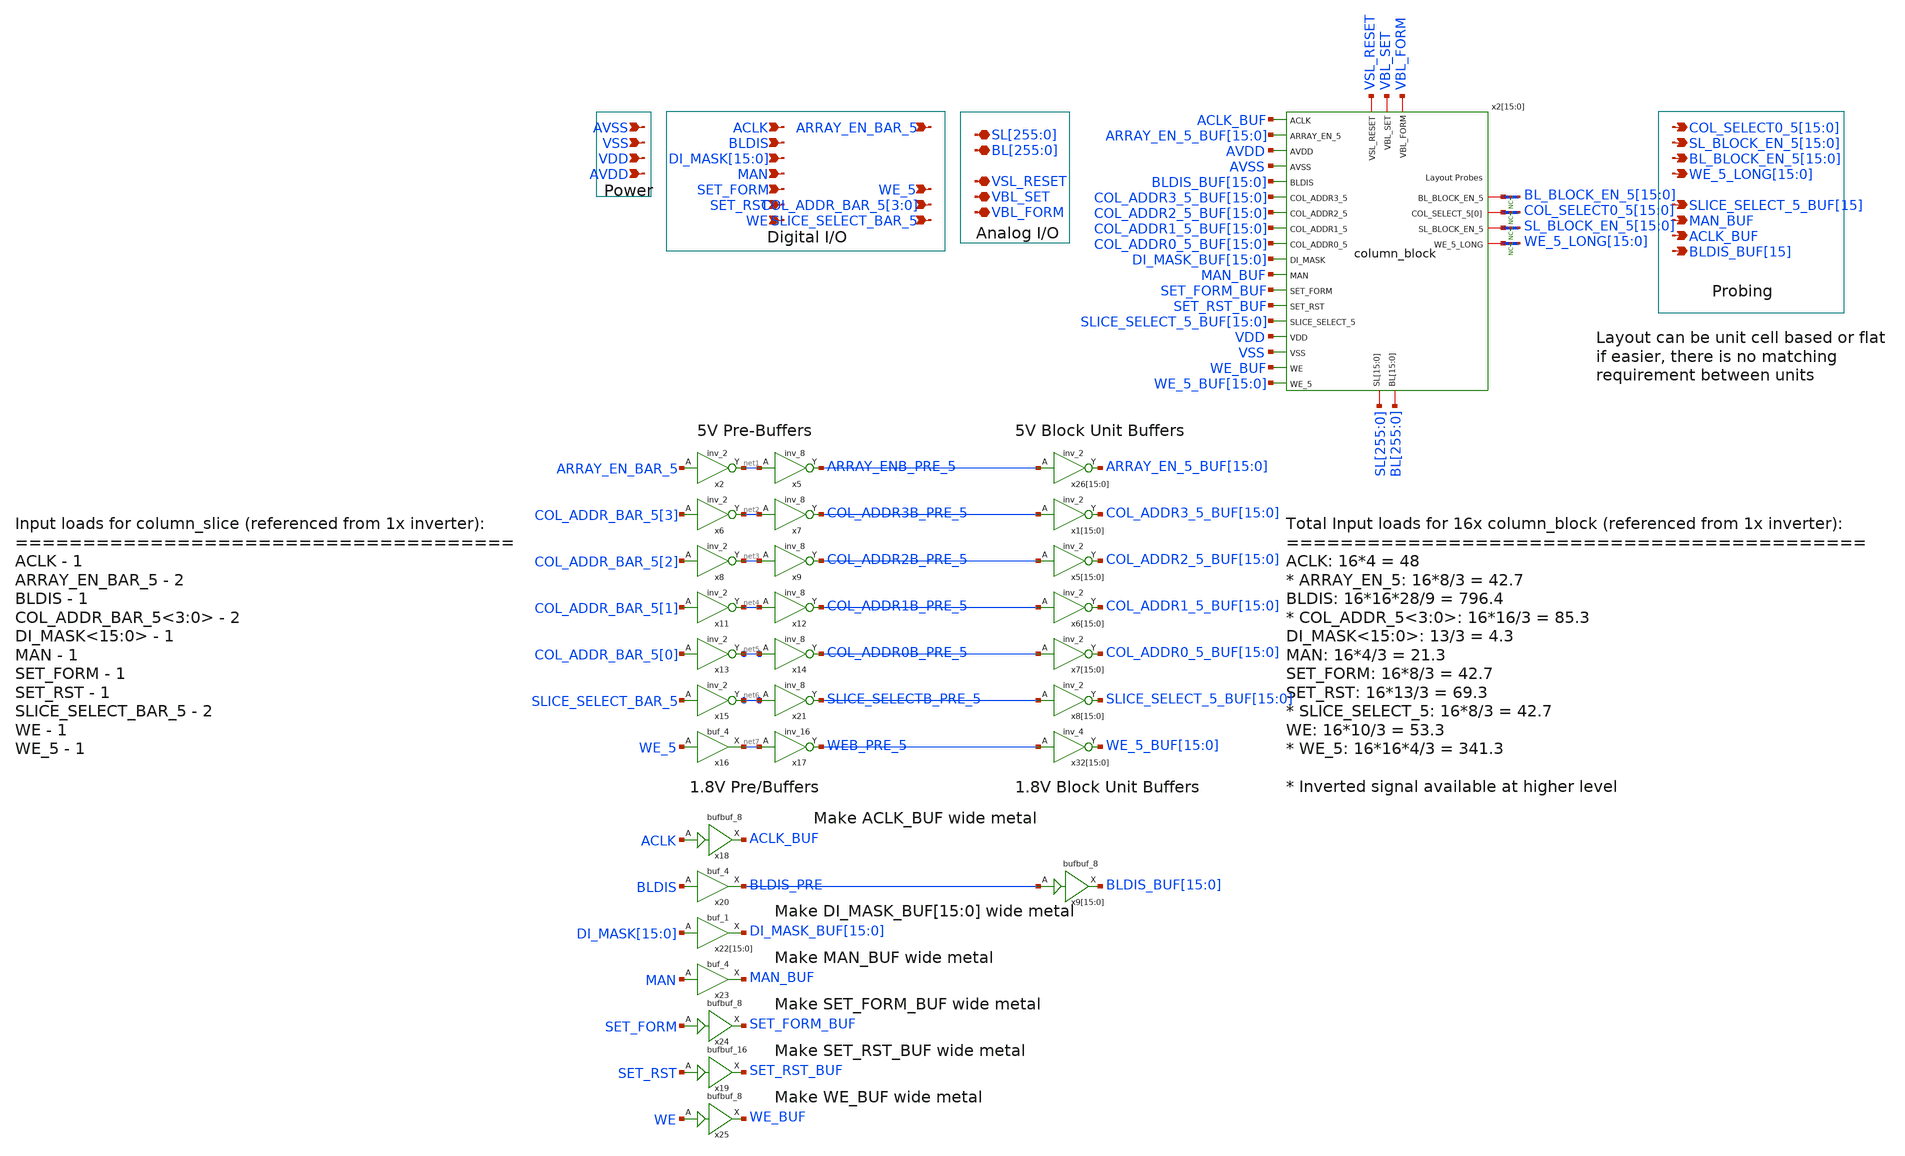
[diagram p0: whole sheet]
** sch_path: BL_SL_Writing_Interface/column_slice.sch
**.subckt column_slice
*+ COL_SELECT0_5[15],COL_SELECT0_5[14],COL_SELECT0_5[13],COL_SELECT0_5[12],COL_SELECT0_5[11],COL_SELECT0_5[10],COL_SELECT0_5[9],COL_SELECT0_5[8],COL_SELECT0_5[7],COL_SELECT0_5[6],COL_SELECT0_5[5],COL_SELECT0_5[4],COL_SELECT0_5[3],COL_SELECT0_5[2],COL_SELECT0_5[1],COL_SELECT0_5[0]
*+ SL_BLOCK_EN_5[15],SL_BLOCK_EN_5[14],SL_BLOCK_EN_5[13],SL_BLOCK_EN_5[12],SL_BLOCK_EN_5[11],SL_BLOCK_EN_5[10],SL_BLOCK_EN_5[9],SL_BLOCK_EN_5[8],SL_BLOCK_EN_5[7],SL_BLOCK_EN_5[6],SL_BLOCK_EN_5[5],SL_BLOCK_EN_5[4],SL_BLOCK_EN_5[3],SL_BLOCK_EN_5[2],SL_BLOCK_EN_5[1],SL_BLOCK_EN_5[0]
*+ BL_BLOCK_EN_5[15],BL_BLOCK_EN_5[14],BL_BLOCK_EN_5[13],BL_BLOCK_EN_5[12],BL_BLOCK_EN_5[11],BL_BLOCK_EN_5[10],BL_BLOCK_EN_5[9],BL_BLOCK_EN_5[8],BL_BLOCK_EN_5[7],BL_BLOCK_EN_5[6],BL_BLOCK_EN_5[5],BL_BLOCK_EN_5[4],BL_BLOCK_EN_5[3],BL_BLOCK_EN_5[2],BL_BLOCK_EN_5[1],BL_BLOCK_EN_5[0]
*+ WE_5_LONG[15],WE_5_LONG[14],WE_5_LONG[13],WE_5_LONG[12],WE_5_LONG[11],WE_5_LONG[10],WE_5_LONG[9],WE_5_LONG[8],WE_5_LONG[7],WE_5_LONG[6],WE_5_LONG[5],WE_5_LONG[4],WE_5_LONG[3],WE_5_LONG[2],WE_5_LONG[1],WE_5_LONG[0] SLICE_SELECT_5_BUF[15] MAN_BUF ACLK_BUF BLDIS_BUF[15]
*+ SL[255],SL[254],SL[253],SL[252],SL[251],SL[250],SL[249],SL[248],SL[247],SL[246],SL[245],SL[244],SL[243],SL[242],SL[241],SL[240],SL[239],SL[238],SL[237],SL[236],SL[235],SL[234],SL[233],SL[232],SL[231],SL[230],SL[229],SL[228],SL[227],SL[226],SL[225],SL[224],SL[223],SL[222],SL[221],SL[220],SL[219],SL[218],SL[217],SL[216],SL[215],SL[214],SL[213],SL[212],SL[211],SL[210],SL[209],SL[208],SL[207],SL[206],SL[205],SL[204],SL[203],SL[202],SL[201],SL[200],SL[199],SL[198],SL[197],SL[196],SL[195],SL[194],SL[193],SL[192],SL[191],SL[190],SL[189],SL[188],SL[187],SL[186],SL[185],SL[184],SL[183],SL[182],SL[181],SL[180],SL[179],SL[178],SL[177],SL[176],SL[175],SL[174],SL[173],SL[172],SL[171],SL[170],SL[169],SL[168],SL[167],SL[166],SL[165],SL[164],SL[163],SL[162],SL[161],SL[160],SL[159],SL[158],SL[157],SL[156],SL[155],SL[154],SL[153],SL[152],SL[151],SL[150],SL[149],SL[148],SL[147],SL[146],SL[145],SL[144],SL[143],SL[142],SL[141],SL[140],SL[139],SL[138],SL[137],SL[136],SL[135],SL[134],SL[133],SL[132],SL[131],SL[130],SL[129],SL[128],SL[127],SL[126],SL[125],SL[124],SL[123],SL[122],SL[121],SL[120],SL[119],SL[118],SL[117],SL[116],SL[115],SL[114],SL[113],SL[112],SL[111],SL[110],SL[109],SL[108],SL[107],SL[106],SL[105],SL[104],SL[103],SL[102],SL[101],SL[100],SL[99],SL[98],SL[97],SL[96],SL[95],SL[94],SL[93],SL[92],SL[91],SL[90],SL[89],SL[88],SL[87],SL[86],SL[85],SL[84],SL[83],SL[82],SL[81],SL[80],SL[79],SL[78],SL[77],SL[76],SL[75],SL[74],SL[73],SL[72],SL[71],SL[70],SL[69],SL[68],SL[67],SL[66],SL[65],SL[64],SL[63],SL[62],SL[61],SL[60],SL[59],SL[58],SL[57],SL[56],SL[55],SL[54],SL[53],SL[52],SL[51],SL[50],SL[49],SL[48],SL[47],SL[46],SL[45],SL[44],SL[43],SL[42],SL[41],SL[40],SL[39],SL[38],SL[37],SL[36],SL[35],SL[34],SL[33],SL[32],SL[31],SL[30],SL[29],SL[28],SL[27],SL[26],SL[25],SL[24],SL[23],SL[22],SL[21],SL[20],SL[19],SL[18],SL[17],SL[16],SL[15],SL[14],SL[13],SL[12],SL[11],SL[10],SL[9],SL[8],SL[7],SL[6],SL[5],SL[4],SL[3],SL[2],SL[1],SL[0]
*+ BL[255],BL[254],BL[253],BL[252],BL[251],BL[250],BL[249],BL[248],BL[247],BL[246],BL[245],BL[244],BL[243],BL[242],BL[241],BL[240],BL[239],BL[238],BL[237],BL[236],BL[235],BL[234],BL[233],BL[232],BL[231],BL[230],BL[229],BL[228],BL[227],BL[226],BL[225],BL[224],BL[223],BL[222],BL[221],BL[220],BL[219],BL[218],BL[217],BL[216],BL[215],BL[214],BL[213],BL[212],BL[211],BL[210],BL[209],BL[208],BL[207],BL[206],BL[205],BL[204],BL[203],BL[202],BL[201],BL[200],BL[199],BL[198],BL[197],BL[196],BL[195],BL[194],BL[193],BL[192],BL[191],BL[190],BL[189],BL[188],BL[187],BL[186],BL[185],BL[184],BL[183],BL[182],BL[181],BL[180],BL[179],BL[178],BL[177],BL[176],BL[175],BL[174],BL[173],BL[172],BL[171],BL[170],BL[169],BL[168],BL[167],BL[166],BL[165],BL[164],BL[163],BL[162],BL[161],BL[160],BL[159],BL[158],BL[157],BL[156],BL[155],BL[154],BL[153],BL[152],BL[151],BL[150],BL[149],BL[148],BL[147],BL[146],BL[145],BL[144],BL[143],BL[142],BL[141],BL[140],BL[139],BL[138],BL[137],BL[136],BL[135],BL[134],BL[133],BL[132],BL[131],BL[130],BL[129],BL[128],BL[127],BL[126],BL[125],BL[124],BL[123],BL[122],BL[121],BL[120],BL[119],BL[118],BL[117],BL[116],BL[115],BL[114],BL[113],BL[112],BL[111],BL[110],BL[109],BL[108],BL[107],BL[106],BL[105],BL[104],BL[103],BL[102],BL[101],BL[100],BL[99],BL[98],BL[97],BL[96],BL[95],BL[94],BL[93],BL[92],BL[91],BL[90],BL[89],BL[88],BL[87],BL[86],BL[85],BL[84],BL[83],BL[82],BL[81],BL[80],BL[79],BL[78],BL[77],BL[76],BL[75],BL[74],BL[73],BL[72],BL[71],BL[70],BL[69],BL[68],BL[67],BL[66],BL[65],BL[64],BL[63],BL[62],BL[61],BL[60],BL[59],BL[58],BL[57],BL[56],BL[55],BL[54],BL[53],BL[52],BL[51],BL[50],BL[49],BL[48],BL[47],BL[46],BL[45],BL[44],BL[43],BL[42],BL[41],BL[40],BL[39],BL[38],BL[37],BL[36],BL[35],BL[34],BL[33],BL[32],BL[31],BL[30],BL[29],BL[28],BL[27],BL[26],BL[25],BL[24],BL[23],BL[22],BL[21],BL[20],BL[19],BL[18],BL[17],BL[16],BL[15],BL[14],BL[13],BL[12],BL[11],BL[10],BL[9],BL[8],BL[7],BL[6],BL[5],BL[4],BL[3],BL[2],BL[1],BL[0] VSL_RESET VBL_SET VBL_FORM AVSS VSS VDD AVDD ACLK ARRAY_EN_BAR_5 BLDIS
*+ COL_ADDR_BAR_5[3],COL_ADDR_BAR_5[2],COL_ADDR_BAR_5[1],COL_ADDR_BAR_5[0]
*+ DI_MASK[15],DI_MASK[14],DI_MASK[13],DI_MASK[12],DI_MASK[11],DI_MASK[10],DI_MASK[9],DI_MASK[8],DI_MASK[7],DI_MASK[6],DI_MASK[5],DI_MASK[4],DI_MASK[3],DI_MASK[2],DI_MASK[1],DI_MASK[0] MAN WE SET_FORM SET_RST WE_5 SLICE_SELECT_BAR_5
*.opin
*+ COL_SELECT0_5[15],COL_SELECT0_5[14],COL_SELECT0_5[13],COL_SELECT0_5[12],COL_SELECT0_5[11],COL_SELECT0_5[10],COL_SELECT0_5[9],COL_SELECT0_5[8],COL_SELECT0_5[7],COL_SELECT0_5[6],COL_SELECT0_5[5],COL_SELECT0_5[4],COL_SELECT0_5[3],COL_SELECT0_5[2],COL_SELECT0_5[1],COL_SELECT0_5[0]
*.opin
*+ SL_BLOCK_EN_5[15],SL_BLOCK_EN_5[14],SL_BLOCK_EN_5[13],SL_BLOCK_EN_5[12],SL_BLOCK_EN_5[11],SL_BLOCK_EN_5[10],SL_BLOCK_EN_5[9],SL_BLOCK_EN_5[8],SL_BLOCK_EN_5[7],SL_BLOCK_EN_5[6],SL_BLOCK_EN_5[5],SL_BLOCK_EN_5[4],SL_BLOCK_EN_5[3],SL_BLOCK_EN_5[2],SL_BLOCK_EN_5[1],SL_BLOCK_EN_5[0]
*.opin
*+ BL_BLOCK_EN_5[15],BL_BLOCK_EN_5[14],BL_BLOCK_EN_5[13],BL_BLOCK_EN_5[12],BL_BLOCK_EN_5[11],BL_BLOCK_EN_5[10],BL_BLOCK_EN_5[9],BL_BLOCK_EN_5[8],BL_BLOCK_EN_5[7],BL_BLOCK_EN_5[6],BL_BLOCK_EN_5[5],BL_BLOCK_EN_5[4],BL_BLOCK_EN_5[3],BL_BLOCK_EN_5[2],BL_BLOCK_EN_5[1],BL_BLOCK_EN_5[0]
*.opin
*+ WE_5_LONG[15],WE_5_LONG[14],WE_5_LONG[13],WE_5_LONG[12],WE_5_LONG[11],WE_5_LONG[10],WE_5_LONG[9],WE_5_LONG[8],WE_5_LONG[7],WE_5_LONG[6],WE_5_LONG[5],WE_5_LONG[4],WE_5_LONG[3],WE_5_LONG[2],WE_5_LONG[1],WE_5_LONG[0]
*.opin SLICE_SELECT_5_BUF[15]
*.opin MAN_BUF
*.opin ACLK_BUF
*.opin BLDIS_BUF[15]
*.iopin
*+ SL[255],SL[254],SL[253],SL[252],SL[251],SL[250],SL[249],SL[248],SL[247],SL[246],SL[245],SL[244],SL[243],SL[242],SL[241],SL[240],SL[239],SL[238],SL[237],SL[236],SL[235],SL[234],SL[233],SL[232],SL[231],SL[230],SL[229],SL[228],SL[227],SL[226],SL[225],SL[224],SL[223],SL[222],SL[221],SL[220],SL[219],SL[218],SL[217],SL[216],SL[215],SL[214],SL[213],SL[212],SL[211],SL[210],SL[209],SL[208],SL[207],SL[206],SL[205],SL[204],SL[203],SL[202],SL[201],SL[200],SL[199],SL[198],SL[197],SL[196],SL[195],SL[194],SL[193],SL[192],SL[191],SL[190],SL[189],SL[188],SL[187],SL[186],SL[185],SL[184],SL[183],SL[182],SL[181],SL[180],SL[179],SL[178],SL[177],SL[176],SL[175],SL[174],SL[173],SL[172],SL[171],SL[170],SL[169],SL[168],SL[167],SL[166],SL[165],SL[164],SL[163],SL[162],SL[161],SL[160],SL[159],SL[158],SL[157],SL[156],SL[155],SL[154],SL[153],SL[152],SL[151],SL[150],SL[149],SL[148],SL[147],SL[146],SL[145],SL[144],SL[143],SL[142],SL[141],SL[140],SL[139],SL[138],SL[137],SL[136],SL[135],SL[134],SL[133],SL[132],SL[131],SL[130],SL[129],SL[128],SL[127],SL[126],SL[125],SL[124],SL[123],SL[122],SL[121],SL[120],SL[119],SL[118],SL[117],SL[116],SL[115],SL[114],SL[113],SL[112],SL[111],SL[110],SL[109],SL[108],SL[107],SL[106],SL[105],SL[104],SL[103],SL[102],SL[101],SL[100],SL[99],SL[98],SL[97],SL[96],SL[95],SL[94],SL[93],SL[92],SL[91],SL[90],SL[89],SL[88],SL[87],SL[86],SL[85],SL[84],SL[83],SL[82],SL[81],SL[80],SL[79],SL[78],SL[77],SL[76],SL[75],SL[74],SL[73],SL[72],SL[71],SL[70],SL[69],SL[68],SL[67],SL[66],SL[65],SL[64],SL[63],SL[62],SL[61],SL[60],SL[59],SL[58],SL[57],SL[56],SL[55],SL[54],SL[53],SL[52],SL[51],SL[50],SL[49],SL[48],SL[47],SL[46],SL[45],SL[44],SL[43],SL[42],SL[41],SL[40],SL[39],SL[38],SL[37],SL[36],SL[35],SL[34],SL[33],SL[32],SL[31],SL[30],SL[29],SL[28],SL[27],SL[26],SL[25],SL[24],SL[23],SL[22],SL[21],SL[20],SL[19],SL[18],SL[17],SL[16],SL[15],SL[14],SL[13],SL[12],SL[11],SL[10],SL[9],SL[8],SL[7],SL[6],SL[5],SL[4],SL[3],SL[2],SL[1],SL[0]
*.iopin
*+ BL[255],BL[254],BL[253],BL[252],BL[251],BL[250],BL[249],BL[248],BL[247],BL[246],BL[245],BL[244],BL[243],BL[242],BL[241],BL[240],BL[239],BL[238],BL[237],BL[236],BL[235],BL[234],BL[233],BL[232],BL[231],BL[230],BL[229],BL[228],BL[227],BL[226],BL[225],BL[224],BL[223],BL[222],BL[221],BL[220],BL[219],BL[218],BL[217],BL[216],BL[215],BL[214],BL[213],BL[212],BL[211],BL[210],BL[209],BL[208],BL[207],BL[206],BL[205],BL[204],BL[203],BL[202],BL[201],BL[200],BL[199],BL[198],BL[197],BL[196],BL[195],BL[194],BL[193],BL[192],BL[191],BL[190],BL[189],BL[188],BL[187],BL[186],BL[185],BL[184],BL[183],BL[182],BL[181],BL[180],BL[179],BL[178],BL[177],BL[176],BL[175],BL[174],BL[173],BL[172],BL[171],BL[170],BL[169],BL[168],BL[167],BL[166],BL[165],BL[164],BL[163],BL[162],BL[161],BL[160],BL[159],BL[158],BL[157],BL[156],BL[155],BL[154],BL[153],BL[152],BL[151],BL[150],BL[149],BL[148],BL[147],BL[146],BL[145],BL[144],BL[143],BL[142],BL[141],BL[140],BL[139],BL[138],BL[137],BL[136],BL[135],BL[134],BL[133],BL[132],BL[131],BL[130],BL[129],BL[128],BL[127],BL[126],BL[125],BL[124],BL[123],BL[122],BL[121],BL[120],BL[119],BL[118],BL[117],BL[116],BL[115],BL[114],BL[113],BL[112],BL[111],BL[110],BL[109],BL[108],BL[107],BL[106],BL[105],BL[104],BL[103],BL[102],BL[101],BL[100],BL[99],BL[98],BL[97],BL[96],BL[95],BL[94],BL[93],BL[92],BL[91],BL[90],BL[89],BL[88],BL[87],BL[86],BL[85],BL[84],BL[83],BL[82],BL[81],BL[80],BL[79],BL[78],BL[77],BL[76],BL[75],BL[74],BL[73],BL[72],BL[71],BL[70],BL[69],BL[68],BL[67],BL[66],BL[65],BL[64],BL[63],BL[62],BL[61],BL[60],BL[59],BL[58],BL[57],BL[56],BL[55],BL[54],BL[53],BL[52],BL[51],BL[50],BL[49],BL[48],BL[47],BL[46],BL[45],BL[44],BL[43],BL[42],BL[41],BL[40],BL[39],BL[38],BL[37],BL[36],BL[35],BL[34],BL[33],BL[32],BL[31],BL[30],BL[29],BL[28],BL[27],BL[26],BL[25],BL[24],BL[23],BL[22],BL[21],BL[20],BL[19],BL[18],BL[17],BL[16],BL[15],BL[14],BL[13],BL[12],BL[11],BL[10],BL[9],BL[8],BL[7],BL[6],BL[5],BL[4],BL[3],BL[2],BL[1],BL[0]
*.iopin VSL_RESET
*.iopin VBL_SET
*.iopin VBL_FORM
*.ipin AVSS
*.ipin VSS
*.ipin VDD
*.ipin AVDD
*.ipin ACLK
*.ipin ARRAY_EN_BAR_5
*.ipin BLDIS
*.ipin COL_ADDR_BAR_5[3],COL_ADDR_BAR_5[2],COL_ADDR_BAR_5[1],COL_ADDR_BAR_5[0]
*.ipin
*+ DI_MASK[15],DI_MASK[14],DI_MASK[13],DI_MASK[12],DI_MASK[11],DI_MASK[10],DI_MASK[9],DI_MASK[8],DI_MASK[7],DI_MASK[6],DI_MASK[5],DI_MASK[4],DI_MASK[3],DI_MASK[2],DI_MASK[1],DI_MASK[0]
*.ipin MAN
*.ipin WE
*.ipin SET_FORM
*.ipin SET_RST
*.ipin WE_5
*.ipin SLICE_SELECT_BAR_5
x2 ARRAY_EN_BAR_5 VSS VSS AVDD AVDD net1 sky130_fd_sc_hvl__inv_2
x5 net1 VSS VSS AVDD AVDD ARRAY_ENB_PRE_5 sky130_fd_sc_hvl__inv_8
x16 WE_5 VSS VSS AVDD AVDD net7 sky130_fd_sc_hvl__buf_4
x17 net7 VSS VSS AVDD AVDD WEB_PRE_5 sky130_fd_sc_hvl__inv_16
x18 ACLK VSS VSS VDD VDD ACLK_BUF sky130_fd_sc_hd__bufbuf_8
x19 SET_RST VSS VSS VDD VDD SET_RST_BUF sky130_fd_sc_hd__bufbuf_16
x6 COL_ADDR_BAR_5[3] VSS VSS AVDD AVDD net2 sky130_fd_sc_hvl__inv_2
x7 net2 VSS VSS AVDD AVDD COL_ADDR3B_PRE_5 sky130_fd_sc_hvl__inv_8
x8 COL_ADDR_BAR_5[2] VSS VSS AVDD AVDD net3 sky130_fd_sc_hvl__inv_2
x9 net3 VSS VSS AVDD AVDD COL_ADDR2B_PRE_5 sky130_fd_sc_hvl__inv_8
x11 COL_ADDR_BAR_5[1] VSS VSS AVDD AVDD net4 sky130_fd_sc_hvl__inv_2
x12 net4 VSS VSS AVDD AVDD COL_ADDR1B_PRE_5 sky130_fd_sc_hvl__inv_8
x13 COL_ADDR_BAR_5[0] VSS VSS AVDD AVDD net5 sky130_fd_sc_hvl__inv_2
x14 net5 VSS VSS AVDD AVDD COL_ADDR0B_PRE_5 sky130_fd_sc_hvl__inv_8
x15 SLICE_SELECT_BAR_5 VSS VSS AVDD AVDD net6 sky130_fd_sc_hvl__inv_2
x21 net6 VSS VSS AVDD AVDD SLICE_SELECTB_PRE_5 sky130_fd_sc_hvl__inv_8
x20 BLDIS VSS VSS VDD VDD BLDIS_PRE sky130_fd_sc_hd__buf_4
x22[15] DI_MASK[15] VSS VSS VDD VDD DI_MASK_BUF[15] sky130_fd_sc_hd__buf_1
x22[14] DI_MASK[14] VSS VSS VDD VDD DI_MASK_BUF[14] sky130_fd_sc_hd__buf_1
x22[13] DI_MASK[13] VSS VSS VDD VDD DI_MASK_BUF[13] sky130_fd_sc_hd__buf_1
x22[12] DI_MASK[12] VSS VSS VDD VDD DI_MASK_BUF[12] sky130_fd_sc_hd__buf_1
x22[11] DI_MASK[11] VSS VSS VDD VDD DI_MASK_BUF[11] sky130_fd_sc_hd__buf_1
x22[10] DI_MASK[10] VSS VSS VDD VDD DI_MASK_BUF[10] sky130_fd_sc_hd__buf_1
x22[9] DI_MASK[9] VSS VSS VDD VDD DI_MASK_BUF[9] sky130_fd_sc_hd__buf_1
x22[8] DI_MASK[8] VSS VSS VDD VDD DI_MASK_BUF[8] sky130_fd_sc_hd__buf_1
x22[7] DI_MASK[7] VSS VSS VDD VDD DI_MASK_BUF[7] sky130_fd_sc_hd__buf_1
x22[6] DI_MASK[6] VSS VSS VDD VDD DI_MASK_BUF[6] sky130_fd_sc_hd__buf_1
x22[5] DI_MASK[5] VSS VSS VDD VDD DI_MASK_BUF[5] sky130_fd_sc_hd__buf_1
x22[4] DI_MASK[4] VSS VSS VDD VDD DI_MASK_BUF[4] sky130_fd_sc_hd__buf_1
x22[3] DI_MASK[3] VSS VSS VDD VDD DI_MASK_BUF[3] sky130_fd_sc_hd__buf_1
x22[2] DI_MASK[2] VSS VSS VDD VDD DI_MASK_BUF[2] sky130_fd_sc_hd__buf_1
x22[1] DI_MASK[1] VSS VSS VDD VDD DI_MASK_BUF[1] sky130_fd_sc_hd__buf_1
x22[0] DI_MASK[0] VSS VSS VDD VDD DI_MASK_BUF[0] sky130_fd_sc_hd__buf_1
x23 MAN VSS VSS VDD VDD MAN_BUF sky130_fd_sc_hd__buf_4
x24 SET_FORM VSS VSS VDD VDD SET_FORM_BUF sky130_fd_sc_hd__bufbuf_8
x25 WE VSS VSS VDD VDD WE_BUF sky130_fd_sc_hd__bufbuf_8
x26[15] ARRAY_ENB_PRE_5 VSS VSS AVDD AVDD ARRAY_EN_5_BUF[15] sky130_fd_sc_hvl__inv_2
x26[14] ARRAY_ENB_PRE_5 VSS VSS AVDD AVDD ARRAY_EN_5_BUF[14] sky130_fd_sc_hvl__inv_2
x26[13] ARRAY_ENB_PRE_5 VSS VSS AVDD AVDD ARRAY_EN_5_BUF[13] sky130_fd_sc_hvl__inv_2
x26[12] ARRAY_ENB_PRE_5 VSS VSS AVDD AVDD ARRAY_EN_5_BUF[12] sky130_fd_sc_hvl__inv_2
x26[11] ARRAY_ENB_PRE_5 VSS VSS AVDD AVDD ARRAY_EN_5_BUF[11] sky130_fd_sc_hvl__inv_2
x26[10] ARRAY_ENB_PRE_5 VSS VSS AVDD AVDD ARRAY_EN_5_BUF[10] sky130_fd_sc_hvl__inv_2
x26[9] ARRAY_ENB_PRE_5 VSS VSS AVDD AVDD ARRAY_EN_5_BUF[9] sky130_fd_sc_hvl__inv_2
x26[8] ARRAY_ENB_PRE_5 VSS VSS AVDD AVDD ARRAY_EN_5_BUF[8] sky130_fd_sc_hvl__inv_2
x26[7] ARRAY_ENB_PRE_5 VSS VSS AVDD AVDD ARRAY_EN_5_BUF[7] sky130_fd_sc_hvl__inv_2
x26[6] ARRAY_ENB_PRE_5 VSS VSS AVDD AVDD ARRAY_EN_5_BUF[6] sky130_fd_sc_hvl__inv_2
x26[5] ARRAY_ENB_PRE_5 VSS VSS AVDD AVDD ARRAY_EN_5_BUF[5] sky130_fd_sc_hvl__inv_2
x26[4] ARRAY_ENB_PRE_5 VSS VSS AVDD AVDD ARRAY_EN_5_BUF[4] sky130_fd_sc_hvl__inv_2
x26[3] ARRAY_ENB_PRE_5 VSS VSS AVDD AVDD ARRAY_EN_5_BUF[3] sky130_fd_sc_hvl__inv_2
x26[2] ARRAY_ENB_PRE_5 VSS VSS AVDD AVDD ARRAY_EN_5_BUF[2] sky130_fd_sc_hvl__inv_2
x26[1] ARRAY_ENB_PRE_5 VSS VSS AVDD AVDD ARRAY_EN_5_BUF[1] sky130_fd_sc_hvl__inv_2
x26[0] ARRAY_ENB_PRE_5 VSS VSS AVDD AVDD ARRAY_EN_5_BUF[0] sky130_fd_sc_hvl__inv_2
x32[15] WEB_PRE_5 VGND VNB VPB VPWR WE_5_BUF[15] sky130_fd_sc_hvl__inv_4
x32[14] WEB_PRE_5 VGND VNB VPB VPWR WE_5_BUF[14] sky130_fd_sc_hvl__inv_4
x32[13] WEB_PRE_5 VGND VNB VPB VPWR WE_5_BUF[13] sky130_fd_sc_hvl__inv_4
x32[12] WEB_PRE_5 VGND VNB VPB VPWR WE_5_BUF[12] sky130_fd_sc_hvl__inv_4
x32[11] WEB_PRE_5 VGND VNB VPB VPWR WE_5_BUF[11] sky130_fd_sc_hvl__inv_4
x32[10] WEB_PRE_5 VGND VNB VPB VPWR WE_5_BUF[10] sky130_fd_sc_hvl__inv_4
x32[9] WEB_PRE_5 VGND VNB VPB VPWR WE_5_BUF[9] sky130_fd_sc_hvl__inv_4
x32[8] WEB_PRE_5 VGND VNB VPB VPWR WE_5_BUF[8] sky130_fd_sc_hvl__inv_4
x32[7] WEB_PRE_5 VGND VNB VPB VPWR WE_5_BUF[7] sky130_fd_sc_hvl__inv_4
x32[6] WEB_PRE_5 VGND VNB VPB VPWR WE_5_BUF[6] sky130_fd_sc_hvl__inv_4
x32[5] WEB_PRE_5 VGND VNB VPB VPWR WE_5_BUF[5] sky130_fd_sc_hvl__inv_4
x32[4] WEB_PRE_5 VGND VNB VPB VPWR WE_5_BUF[4] sky130_fd_sc_hvl__inv_4
x32[3] WEB_PRE_5 VGND VNB VPB VPWR WE_5_BUF[3] sky130_fd_sc_hvl__inv_4
x32[2] WEB_PRE_5 VGND VNB VPB VPWR WE_5_BUF[2] sky130_fd_sc_hvl__inv_4
x32[1] WEB_PRE_5 VGND VNB VPB VPWR WE_5_BUF[1] sky130_fd_sc_hvl__inv_4
x32[0] WEB_PRE_5 VGND VNB VPB VPWR WE_5_BUF[0] sky130_fd_sc_hvl__inv_4
x1[15] COL_ADDR3B_PRE_5 VSS VSS AVDD AVDD COL_ADDR3_5_BUF[15] sky130_fd_sc_hvl__inv_2
x1[14] COL_ADDR3B_PRE_5 VSS VSS AVDD AVDD COL_ADDR3_5_BUF[14] sky130_fd_sc_hvl__inv_2
x1[13] COL_ADDR3B_PRE_5 VSS VSS AVDD AVDD COL_ADDR3_5_BUF[13] sky130_fd_sc_hvl__inv_2
x1[12] COL_ADDR3B_PRE_5 VSS VSS AVDD AVDD COL_ADDR3_5_BUF[12] sky130_fd_sc_hvl__inv_2
x1[11] COL_ADDR3B_PRE_5 VSS VSS AVDD AVDD COL_ADDR3_5_BUF[11] sky130_fd_sc_hvl__inv_2
x1[10] COL_ADDR3B_PRE_5 VSS VSS AVDD AVDD COL_ADDR3_5_BUF[10] sky130_fd_sc_hvl__inv_2
x1[9] COL_ADDR3B_PRE_5 VSS VSS AVDD AVDD COL_ADDR3_5_BUF[9] sky130_fd_sc_hvl__inv_2
x1[8] COL_ADDR3B_PRE_5 VSS VSS AVDD AVDD COL_ADDR3_5_BUF[8] sky130_fd_sc_hvl__inv_2
x1[7] COL_ADDR3B_PRE_5 VSS VSS AVDD AVDD COL_ADDR3_5_BUF[7] sky130_fd_sc_hvl__inv_2
x1[6] COL_ADDR3B_PRE_5 VSS VSS AVDD AVDD COL_ADDR3_5_BUF[6] sky130_fd_sc_hvl__inv_2
x1[5] COL_ADDR3B_PRE_5 VSS VSS AVDD AVDD COL_ADDR3_5_BUF[5] sky130_fd_sc_hvl__inv_2
x1[4] COL_ADDR3B_PRE_5 VSS VSS AVDD AVDD COL_ADDR3_5_BUF[4] sky130_fd_sc_hvl__inv_2
x1[3] COL_ADDR3B_PRE_5 VSS VSS AVDD AVDD COL_ADDR3_5_BUF[3] sky130_fd_sc_hvl__inv_2
x1[2] COL_ADDR3B_PRE_5 VSS VSS AVDD AVDD COL_ADDR3_5_BUF[2] sky130_fd_sc_hvl__inv_2
x1[1] COL_ADDR3B_PRE_5 VSS VSS AVDD AVDD COL_ADDR3_5_BUF[1] sky130_fd_sc_hvl__inv_2
x1[0] COL_ADDR3B_PRE_5 VSS VSS AVDD AVDD COL_ADDR3_5_BUF[0] sky130_fd_sc_hvl__inv_2
x5[15] COL_ADDR2B_PRE_5 VSS VSS AVDD AVDD COL_ADDR2_5_BUF[15] sky130_fd_sc_hvl__inv_2
x5[14] COL_ADDR2B_PRE_5 VSS VSS AVDD AVDD COL_ADDR2_5_BUF[14] sky130_fd_sc_hvl__inv_2
x5[13] COL_ADDR2B_PRE_5 VSS VSS AVDD AVDD COL_ADDR2_5_BUF[13] sky130_fd_sc_hvl__inv_2
x5[12] COL_ADDR2B_PRE_5 VSS VSS AVDD AVDD COL_ADDR2_5_BUF[12] sky130_fd_sc_hvl__inv_2
x5[11] COL_ADDR2B_PRE_5 VSS VSS AVDD AVDD COL_ADDR2_5_BUF[11] sky130_fd_sc_hvl__inv_2
x5[10] COL_ADDR2B_PRE_5 VSS VSS AVDD AVDD COL_ADDR2_5_BUF[10] sky130_fd_sc_hvl__inv_2
x5[9] COL_ADDR2B_PRE_5 VSS VSS AVDD AVDD COL_ADDR2_5_BUF[9] sky130_fd_sc_hvl__inv_2
x5[8] COL_ADDR2B_PRE_5 VSS VSS AVDD AVDD COL_ADDR2_5_BUF[8] sky130_fd_sc_hvl__inv_2
x5[7] COL_ADDR2B_PRE_5 VSS VSS AVDD AVDD COL_ADDR2_5_BUF[7] sky130_fd_sc_hvl__inv_2
x5[6] COL_ADDR2B_PRE_5 VSS VSS AVDD AVDD COL_ADDR2_5_BUF[6] sky130_fd_sc_hvl__inv_2
x5[5] COL_ADDR2B_PRE_5 VSS VSS AVDD AVDD COL_ADDR2_5_BUF[5] sky130_fd_sc_hvl__inv_2
x5[4] COL_ADDR2B_PRE_5 VSS VSS AVDD AVDD COL_ADDR2_5_BUF[4] sky130_fd_sc_hvl__inv_2
x5[3] COL_ADDR2B_PRE_5 VSS VSS AVDD AVDD COL_ADDR2_5_BUF[3] sky130_fd_sc_hvl__inv_2
x5[2] COL_ADDR2B_PRE_5 VSS VSS AVDD AVDD COL_ADDR2_5_BUF[2] sky130_fd_sc_hvl__inv_2
x5[1] COL_ADDR2B_PRE_5 VSS VSS AVDD AVDD COL_ADDR2_5_BUF[1] sky130_fd_sc_hvl__inv_2
x5[0] COL_ADDR2B_PRE_5 VSS VSS AVDD AVDD COL_ADDR2_5_BUF[0] sky130_fd_sc_hvl__inv_2
x6[15] COL_ADDR1B_PRE_5 VSS VSS AVDD AVDD COL_ADDR1_5_BUF[15] sky130_fd_sc_hvl__inv_2
x6[14] COL_ADDR1B_PRE_5 VSS VSS AVDD AVDD COL_ADDR1_5_BUF[14] sky130_fd_sc_hvl__inv_2
x6[13] COL_ADDR1B_PRE_5 VSS VSS AVDD AVDD COL_ADDR1_5_BUF[13] sky130_fd_sc_hvl__inv_2
x6[12] COL_ADDR1B_PRE_5 VSS VSS AVDD AVDD COL_ADDR1_5_BUF[12] sky130_fd_sc_hvl__inv_2
x6[11] COL_ADDR1B_PRE_5 VSS VSS AVDD AVDD COL_ADDR1_5_BUF[11] sky130_fd_sc_hvl__inv_2
x6[10] COL_ADDR1B_PRE_5 VSS VSS AVDD AVDD COL_ADDR1_5_BUF[10] sky130_fd_sc_hvl__inv_2
x6[9] COL_ADDR1B_PRE_5 VSS VSS AVDD AVDD COL_ADDR1_5_BUF[9] sky130_fd_sc_hvl__inv_2
x6[8] COL_ADDR1B_PRE_5 VSS VSS AVDD AVDD COL_ADDR1_5_BUF[8] sky130_fd_sc_hvl__inv_2
x6[7] COL_ADDR1B_PRE_5 VSS VSS AVDD AVDD COL_ADDR1_5_BUF[7] sky130_fd_sc_hvl__inv_2
x6[6] COL_ADDR1B_PRE_5 VSS VSS AVDD AVDD COL_ADDR1_5_BUF[6] sky130_fd_sc_hvl__inv_2
x6[5] COL_ADDR1B_PRE_5 VSS VSS AVDD AVDD COL_ADDR1_5_BUF[5] sky130_fd_sc_hvl__inv_2
x6[4] COL_ADDR1B_PRE_5 VSS VSS AVDD AVDD COL_ADDR1_5_BUF[4] sky130_fd_sc_hvl__inv_2
x6[3] COL_ADDR1B_PRE_5 VSS VSS AVDD AVDD COL_ADDR1_5_BUF[3] sky130_fd_sc_hvl__inv_2
x6[2] COL_ADDR1B_PRE_5 VSS VSS AVDD AVDD COL_ADDR1_5_BUF[2] sky130_fd_sc_hvl__inv_2
x6[1] COL_ADDR1B_PRE_5 VSS VSS AVDD AVDD COL_ADDR1_5_BUF[1] sky130_fd_sc_hvl__inv_2
x6[0] COL_ADDR1B_PRE_5 VSS VSS AVDD AVDD COL_ADDR1_5_BUF[0] sky130_fd_sc_hvl__inv_2
x7[15] COL_ADDR0B_PRE_5 VSS VSS AVDD AVDD COL_ADDR0_5_BUF[15] sky130_fd_sc_hvl__inv_2
x7[14] COL_ADDR0B_PRE_5 VSS VSS AVDD AVDD COL_ADDR0_5_BUF[14] sky130_fd_sc_hvl__inv_2
x7[13] COL_ADDR0B_PRE_5 VSS VSS AVDD AVDD COL_ADDR0_5_BUF[13] sky130_fd_sc_hvl__inv_2
x7[12] COL_ADDR0B_PRE_5 VSS VSS AVDD AVDD COL_ADDR0_5_BUF[12] sky130_fd_sc_hvl__inv_2
x7[11] COL_ADDR0B_PRE_5 VSS VSS AVDD AVDD COL_ADDR0_5_BUF[11] sky130_fd_sc_hvl__inv_2
x7[10] COL_ADDR0B_PRE_5 VSS VSS AVDD AVDD COL_ADDR0_5_BUF[10] sky130_fd_sc_hvl__inv_2
x7[9] COL_ADDR0B_PRE_5 VSS VSS AVDD AVDD COL_ADDR0_5_BUF[9] sky130_fd_sc_hvl__inv_2
x7[8] COL_ADDR0B_PRE_5 VSS VSS AVDD AVDD COL_ADDR0_5_BUF[8] sky130_fd_sc_hvl__inv_2
x7[7] COL_ADDR0B_PRE_5 VSS VSS AVDD AVDD COL_ADDR0_5_BUF[7] sky130_fd_sc_hvl__inv_2
x7[6] COL_ADDR0B_PRE_5 VSS VSS AVDD AVDD COL_ADDR0_5_BUF[6] sky130_fd_sc_hvl__inv_2
x7[5] COL_ADDR0B_PRE_5 VSS VSS AVDD AVDD COL_ADDR0_5_BUF[5] sky130_fd_sc_hvl__inv_2
x7[4] COL_ADDR0B_PRE_5 VSS VSS AVDD AVDD COL_ADDR0_5_BUF[4] sky130_fd_sc_hvl__inv_2
x7[3] COL_ADDR0B_PRE_5 VSS VSS AVDD AVDD COL_ADDR0_5_BUF[3] sky130_fd_sc_hvl__inv_2
x7[2] COL_ADDR0B_PRE_5 VSS VSS AVDD AVDD COL_ADDR0_5_BUF[2] sky130_fd_sc_hvl__inv_2
x7[1] COL_ADDR0B_PRE_5 VSS VSS AVDD AVDD COL_ADDR0_5_BUF[1] sky130_fd_sc_hvl__inv_2
x7[0] COL_ADDR0B_PRE_5 VSS VSS AVDD AVDD COL_ADDR0_5_BUF[0] sky130_fd_sc_hvl__inv_2
x8[15] SLICE_SELECTB_PRE_5 VSS VSS AVDD AVDD SLICE_SELECT_5_BUF[15] sky130_fd_sc_hvl__inv_2
x8[14] SLICE_SELECTB_PRE_5 VSS VSS AVDD AVDD SLICE_SELECT_5_BUF[14] sky130_fd_sc_hvl__inv_2
x8[13] SLICE_SELECTB_PRE_5 VSS VSS AVDD AVDD SLICE_SELECT_5_BUF[13] sky130_fd_sc_hvl__inv_2
x8[12] SLICE_SELECTB_PRE_5 VSS VSS AVDD AVDD SLICE_SELECT_5_BUF[12] sky130_fd_sc_hvl__inv_2
x8[11] SLICE_SELECTB_PRE_5 VSS VSS AVDD AVDD SLICE_SELECT_5_BUF[11] sky130_fd_sc_hvl__inv_2
x8[10] SLICE_SELECTB_PRE_5 VSS VSS AVDD AVDD SLICE_SELECT_5_BUF[10] sky130_fd_sc_hvl__inv_2
x8[9] SLICE_SELECTB_PRE_5 VSS VSS AVDD AVDD SLICE_SELECT_5_BUF[9] sky130_fd_sc_hvl__inv_2
x8[8] SLICE_SELECTB_PRE_5 VSS VSS AVDD AVDD SLICE_SELECT_5_BUF[8] sky130_fd_sc_hvl__inv_2
x8[7] SLICE_SELECTB_PRE_5 VSS VSS AVDD AVDD SLICE_SELECT_5_BUF[7] sky130_fd_sc_hvl__inv_2
x8[6] SLICE_SELECTB_PRE_5 VSS VSS AVDD AVDD SLICE_SELECT_5_BUF[6] sky130_fd_sc_hvl__inv_2
x8[5] SLICE_SELECTB_PRE_5 VSS VSS AVDD AVDD SLICE_SELECT_5_BUF[5] sky130_fd_sc_hvl__inv_2
x8[4] SLICE_SELECTB_PRE_5 VSS VSS AVDD AVDD SLICE_SELECT_5_BUF[4] sky130_fd_sc_hvl__inv_2
x8[3] SLICE_SELECTB_PRE_5 VSS VSS AVDD AVDD SLICE_SELECT_5_BUF[3] sky130_fd_sc_hvl__inv_2
x8[2] SLICE_SELECTB_PRE_5 VSS VSS AVDD AVDD SLICE_SELECT_5_BUF[2] sky130_fd_sc_hvl__inv_2
x8[1] SLICE_SELECTB_PRE_5 VSS VSS AVDD AVDD SLICE_SELECT_5_BUF[1] sky130_fd_sc_hvl__inv_2
x8[0] SLICE_SELECTB_PRE_5 VSS VSS AVDD AVDD SLICE_SELECT_5_BUF[0] sky130_fd_sc_hvl__inv_2
x9[15] BLDIS_PRE VSS VSS VDD VDD BLDIS_BUF[15] sky130_fd_sc_hd__bufbuf_8
x9[14] BLDIS_PRE VSS VSS VDD VDD BLDIS_BUF[14] sky130_fd_sc_hd__bufbuf_8
x9[13] BLDIS_PRE VSS VSS VDD VDD BLDIS_BUF[13] sky130_fd_sc_hd__bufbuf_8
x9[12] BLDIS_PRE VSS VSS VDD VDD BLDIS_BUF[12] sky130_fd_sc_hd__bufbuf_8
x9[11] BLDIS_PRE VSS VSS VDD VDD BLDIS_BUF[11] sky130_fd_sc_hd__bufbuf_8
x9[10] BLDIS_PRE VSS VSS VDD VDD BLDIS_BUF[10] sky130_fd_sc_hd__bufbuf_8
x9[9] BLDIS_PRE VSS VSS VDD VDD BLDIS_BUF[9] sky130_fd_sc_hd__bufbuf_8
x9[8] BLDIS_PRE VSS VSS VDD VDD BLDIS_BUF[8] sky130_fd_sc_hd__bufbuf_8
x9[7] BLDIS_PRE VSS VSS VDD VDD BLDIS_BUF[7] sky130_fd_sc_hd__bufbuf_8
x9[6] BLDIS_PRE VSS VSS VDD VDD BLDIS_BUF[6] sky130_fd_sc_hd__bufbuf_8
x9[5] BLDIS_PRE VSS VSS VDD VDD BLDIS_BUF[5] sky130_fd_sc_hd__bufbuf_8
x9[4] BLDIS_PRE VSS VSS VDD VDD BLDIS_BUF[4] sky130_fd_sc_hd__bufbuf_8
x9[3] BLDIS_PRE VSS VSS VDD VDD BLDIS_BUF[3] sky130_fd_sc_hd__bufbuf_8
x9[2] BLDIS_PRE VSS VSS VDD VDD BLDIS_BUF[2] sky130_fd_sc_hd__bufbuf_8
x9[1] BLDIS_PRE VSS VSS VDD VDD BLDIS_BUF[1] sky130_fd_sc_hd__bufbuf_8
x9[0] BLDIS_PRE VSS VSS VDD VDD BLDIS_BUF[0] sky130_fd_sc_hd__bufbuf_8
x2[15] VBL_SET DI_MASK_BUF[15] VDD SLICE_SELECT_5_BUF[15] AVDD VBL_FORM COL_ADDR3_5_BUF[15]
+ BLDIS_BUF[15] ACLK_BUF COL_ADDR2_5_BUF[15] VSL_RESET AVSS COL_ADDR1_5_BUF[15] BL[255] BL[254] BL[253] BL[252]
+ BL[251] BL[250] BL[249] BL[248] BL[247] BL[246] BL[245] BL[244] BL[243] BL[242] BL[241] BL[240] VSS
+ SET_FORM_BUF COL_SELECT0_5[15] SL[255] SL[254] SL[253] SL[252] SL[251] SL[250] SL[249] SL[248] SL[247] SL[246]
+ SL[245] SL[244] SL[243] SL[242] SL[241] SL[240] SET_RST_BUF COL_ADDR0_5_BUF[15] SL_BLOCK_EN_5[15]
+ ARRAY_EN_5_BUF[15] MAN_BUF BL_BLOCK_EN_5[15] WE_BUF WE_5_BUF[15] WE_5_LONG[15] column_block
x2[14] VBL_SET DI_MASK_BUF[14] VDD SLICE_SELECT_5_BUF[14] AVDD VBL_FORM COL_ADDR3_5_BUF[14]
+ BLDIS_BUF[14] ACLK_BUF COL_ADDR2_5_BUF[14] VSL_RESET AVSS COL_ADDR1_5_BUF[14] BL[239] BL[238] BL[237] BL[236]
+ BL[235] BL[234] BL[233] BL[232] BL[231] BL[230] BL[229] BL[228] BL[227] BL[226] BL[225] BL[224] VSS
+ SET_FORM_BUF COL_SELECT0_5[14] SL[239] SL[238] SL[237] SL[236] SL[235] SL[234] SL[233] SL[232] SL[231] SL[230]
+ SL[229] SL[228] SL[227] SL[226] SL[225] SL[224] SET_RST_BUF COL_ADDR0_5_BUF[14] SL_BLOCK_EN_5[14]
+ ARRAY_EN_5_BUF[14] MAN_BUF BL_BLOCK_EN_5[14] WE_BUF WE_5_BUF[14] WE_5_LONG[14] column_block
x2[13] VBL_SET DI_MASK_BUF[13] VDD SLICE_SELECT_5_BUF[13] AVDD VBL_FORM COL_ADDR3_5_BUF[13]
+ BLDIS_BUF[13] ACLK_BUF COL_ADDR2_5_BUF[13] VSL_RESET AVSS COL_ADDR1_5_BUF[13] BL[223] BL[222] BL[221] BL[220]
+ BL[219] BL[218] BL[217] BL[216] BL[215] BL[214] BL[213] BL[212] BL[211] BL[210] BL[209] BL[208] VSS
+ SET_FORM_BUF COL_SELECT0_5[13] SL[223] SL[222] SL[221] SL[220] SL[219] SL[218] SL[217] SL[216] SL[215] SL[214]
+ SL[213] SL[212] SL[211] SL[210] SL[209] SL[208] SET_RST_BUF COL_ADDR0_5_BUF[13] SL_BLOCK_EN_5[13]
+ ARRAY_EN_5_BUF[13] MAN_BUF BL_BLOCK_EN_5[13] WE_BUF WE_5_BUF[13] WE_5_LONG[13] column_block
x2[12] VBL_SET DI_MASK_BUF[12] VDD SLICE_SELECT_5_BUF[12] AVDD VBL_FORM COL_ADDR3_5_BUF[12]
+ BLDIS_BUF[12] ACLK_BUF COL_ADDR2_5_BUF[12] VSL_RESET AVSS COL_ADDR1_5_BUF[12] BL[207] BL[206] BL[205] BL[204]
+ BL[203] BL[202] BL[201] BL[200] BL[199] BL[198] BL[197] BL[196] BL[195] BL[194] BL[193] BL[192] VSS
+ SET_FORM_BUF COL_SELECT0_5[12] SL[207] SL[206] SL[205] SL[204] SL[203] SL[202] SL[201] SL[200] SL[199] SL[198]
+ SL[197] SL[196] SL[195] SL[194] SL[193] SL[192] SET_RST_BUF COL_ADDR0_5_BUF[12] SL_BLOCK_EN_5[12]
+ ARRAY_EN_5_BUF[12] MAN_BUF BL_BLOCK_EN_5[12] WE_BUF WE_5_BUF[12] WE_5_LONG[12] column_block
x2[11] VBL_SET DI_MASK_BUF[11] VDD SLICE_SELECT_5_BUF[11] AVDD VBL_FORM COL_ADDR3_5_BUF[11]
+ BLDIS_BUF[11] ACLK_BUF COL_ADDR2_5_BUF[11] VSL_RESET AVSS COL_ADDR1_5_BUF[11] BL[191] BL[190] BL[189] BL[188]
+ BL[187] BL[186] BL[185] BL[184] BL[183] BL[182] BL[181] BL[180] BL[179] BL[178] BL[177] BL[176] VSS
+ SET_FORM_BUF COL_SELECT0_5[11] SL[191] SL[190] SL[189] SL[188] SL[187] SL[186] SL[185] SL[184] SL[183] SL[182]
+ SL[181] SL[180] SL[179] SL[178] SL[177] SL[176] SET_RST_BUF COL_ADDR0_5_BUF[11] SL_BLOCK_EN_5[11]
+ ARRAY_EN_5_BUF[11] MAN_BUF BL_BLOCK_EN_5[11] WE_BUF WE_5_BUF[11] WE_5_LONG[11] column_block
x2[10] VBL_SET DI_MASK_BUF[10] VDD SLICE_SELECT_5_BUF[10] AVDD VBL_FORM COL_ADDR3_5_BUF[10]
+ BLDIS_BUF[10] ACLK_BUF COL_ADDR2_5_BUF[10] VSL_RESET AVSS COL_ADDR1_5_BUF[10] BL[175] BL[174] BL[173] BL[172]
+ BL[171] BL[170] BL[169] BL[168] BL[167] BL[166] BL[165] BL[164] BL[163] BL[162] BL[161] BL[160] VSS
+ SET_FORM_BUF COL_SELECT0_5[10] SL[175] SL[174] SL[173] SL[172] SL[171] SL[170] SL[169] SL[168] SL[167] SL[166]
+ SL[165] SL[164] SL[163] SL[162] SL[161] SL[160] SET_RST_BUF COL_ADDR0_5_BUF[10] SL_BLOCK_EN_5[10]
+ ARRAY_EN_5_BUF[10] MAN_BUF BL_BLOCK_EN_5[10] WE_BUF WE_5_BUF[10] WE_5_LONG[10] column_block
x2[9] VBL_SET DI_MASK_BUF[9] VDD SLICE_SELECT_5_BUF[9] AVDD VBL_FORM COL_ADDR3_5_BUF[9] BLDIS_BUF[9]
+ ACLK_BUF COL_ADDR2_5_BUF[9] VSL_RESET AVSS COL_ADDR1_5_BUF[9] BL[159] BL[158] BL[157] BL[156] BL[155]
+ BL[154] BL[153] BL[152] BL[151] BL[150] BL[149] BL[148] BL[147] BL[146] BL[145] BL[144] VSS SET_FORM_BUF
+ COL_SELECT0_5[9] SL[159] SL[158] SL[157] SL[156] SL[155] SL[154] SL[153] SL[152] SL[151] SL[150] SL[149] SL[148]
+ SL[147] SL[146] SL[145] SL[144] SET_RST_BUF COL_ADDR0_5_BUF[9] SL_BLOCK_EN_5[9] ARRAY_EN_5_BUF[9] MAN_BUF
+ BL_BLOCK_EN_5[9] WE_BUF WE_5_BUF[9] WE_5_LONG[9] column_block
x2[8] VBL_SET DI_MASK_BUF[8] VDD SLICE_SELECT_5_BUF[8] AVDD VBL_FORM COL_ADDR3_5_BUF[8] BLDIS_BUF[8]
+ ACLK_BUF COL_ADDR2_5_BUF[8] VSL_RESET AVSS COL_ADDR1_5_BUF[8] BL[143] BL[142] BL[141] BL[140] BL[139]
+ BL[138] BL[137] BL[136] BL[135] BL[134] BL[133] BL[132] BL[131] BL[130] BL[129] BL[128] VSS SET_FORM_BUF
+ COL_SELECT0_5[8] SL[143] SL[142] SL[141] SL[140] SL[139] SL[138] SL[137] SL[136] SL[135] SL[134] SL[133] SL[132]
+ SL[131] SL[130] SL[129] SL[128] SET_RST_BUF COL_ADDR0_5_BUF[8] SL_BLOCK_EN_5[8] ARRAY_EN_5_BUF[8] MAN_BUF
+ BL_BLOCK_EN_5[8] WE_BUF WE_5_BUF[8] WE_5_LONG[8] column_block
x2[7] VBL_SET DI_MASK_BUF[7] VDD SLICE_SELECT_5_BUF[7] AVDD VBL_FORM COL_ADDR3_5_BUF[7] BLDIS_BUF[7]
+ ACLK_BUF COL_ADDR2_5_BUF[7] VSL_RESET AVSS COL_ADDR1_5_BUF[7] BL[127] BL[126] BL[125] BL[124] BL[123]
+ BL[122] BL[121] BL[120] BL[119] BL[118] BL[117] BL[116] BL[115] BL[114] BL[113] BL[112] VSS SET_FORM_BUF
+ COL_SELECT0_5[7] SL[127] SL[126] SL[125] SL[124] SL[123] SL[122] SL[121] SL[120] SL[119] SL[118] SL[117] SL[116]
+ SL[115] SL[114] SL[113] SL[112] SET_RST_BUF COL_ADDR0_5_BUF[7] SL_BLOCK_EN_5[7] ARRAY_EN_5_BUF[7] MAN_BUF
+ BL_BLOCK_EN_5[7] WE_BUF WE_5_BUF[7] WE_5_LONG[7] column_block
x2[6] VBL_SET DI_MASK_BUF[6] VDD SLICE_SELECT_5_BUF[6] AVDD VBL_FORM COL_ADDR3_5_BUF[6] BLDIS_BUF[6]
+ ACLK_BUF COL_ADDR2_5_BUF[6] VSL_RESET AVSS COL_ADDR1_5_BUF[6] BL[111] BL[110] BL[109] BL[108] BL[107]
+ BL[106] BL[105] BL[104] BL[103] BL[102] BL[101] BL[100] BL[99] BL[98] BL[97] BL[96] VSS SET_FORM_BUF
+ COL_SELECT0_5[6] SL[111] SL[110] SL[109] SL[108] SL[107] SL[106] SL[105] SL[104] SL[103] SL[102] SL[101] SL[100]
+ SL[99] SL[98] SL[97] SL[96] SET_RST_BUF COL_ADDR0_5_BUF[6] SL_BLOCK_EN_5[6] ARRAY_EN_5_BUF[6] MAN_BUF
+ BL_BLOCK_EN_5[6] WE_BUF WE_5_BUF[6] WE_5_LONG[6] column_block
x2[5] VBL_SET DI_MASK_BUF[5] VDD SLICE_SELECT_5_BUF[5] AVDD VBL_FORM COL_ADDR3_5_BUF[5] BLDIS_BUF[5]
+ ACLK_BUF COL_ADDR2_5_BUF[5] VSL_RESET AVSS COL_ADDR1_5_BUF[5] BL[95] BL[94] BL[93] BL[92] BL[91] BL[90]
+ BL[89] BL[88] BL[87] BL[86] BL[85] BL[84] BL[83] BL[82] BL[81] BL[80] VSS SET_FORM_BUF COL_SELECT0_5[5]
+ SL[95] SL[94] SL[93] SL[92] SL[91] SL[90] SL[89] SL[88] SL[87] SL[86] SL[85] SL[84] SL[83] SL[82] SL[81]
+ SL[80] SET_RST_BUF COL_ADDR0_5_BUF[5] SL_BLOCK_EN_5[5] ARRAY_EN_5_BUF[5] MAN_BUF BL_BLOCK_EN_5[5] WE_BUF
+ WE_5_BUF[5] WE_5_LONG[5] column_block
x2[4] VBL_SET DI_MASK_BUF[4] VDD SLICE_SELECT_5_BUF[4] AVDD VBL_FORM COL_ADDR3_5_BUF[4] BLDIS_BUF[4]
+ ACLK_BUF COL_ADDR2_5_BUF[4] VSL_RESET AVSS COL_ADDR1_5_BUF[4] BL[79] BL[78] BL[77] BL[76] BL[75] BL[74]
+ BL[73] BL[72] BL[71] BL[70] BL[69] BL[68] BL[67] BL[66] BL[65] BL[64] VSS SET_FORM_BUF COL_SELECT0_5[4]
+ SL[79] SL[78] SL[77] SL[76] SL[75] SL[74] SL[73] SL[72] SL[71] SL[70] SL[69] SL[68] SL[67] SL[66] SL[65]
+ SL[64] SET_RST_BUF COL_ADDR0_5_BUF[4] SL_BLOCK_EN_5[4] ARRAY_EN_5_BUF[4] MAN_BUF BL_BLOCK_EN_5[4] WE_BUF
+ WE_5_BUF[4] WE_5_LONG[4] column_block
x2[3] VBL_SET DI_MASK_BUF[3] VDD SLICE_SELECT_5_BUF[3] AVDD VBL_FORM COL_ADDR3_5_BUF[3] BLDIS_BUF[3]
+ ACLK_BUF COL_ADDR2_5_BUF[3] VSL_RESET AVSS COL_ADDR1_5_BUF[3] BL[63] BL[62] BL[61] BL[60] BL[59] BL[58]
+ BL[57] BL[56] BL[55] BL[54] BL[53] BL[52] BL[51] BL[50] BL[49] BL[48] VSS SET_FORM_BUF COL_SELECT0_5[3]
+ SL[63] SL[62] SL[61] SL[60] SL[59] SL[58] SL[57] SL[56] SL[55] SL[54] SL[53] SL[52] SL[51] SL[50] SL[49]
+ SL[48] SET_RST_BUF COL_ADDR0_5_BUF[3] SL_BLOCK_EN_5[3] ARRAY_EN_5_BUF[3] MAN_BUF BL_BLOCK_EN_5[3] WE_BUF
+ WE_5_BUF[3] WE_5_LONG[3] column_block
x2[2] VBL_SET DI_MASK_BUF[2] VDD SLICE_SELECT_5_BUF[2] AVDD VBL_FORM COL_ADDR3_5_BUF[2] BLDIS_BUF[2]
+ ACLK_BUF COL_ADDR2_5_BUF[2] VSL_RESET AVSS COL_ADDR1_5_BUF[2] BL[47] BL[46] BL[45] BL[44] BL[43] BL[42]
+ BL[41] BL[40] BL[39] BL[38] BL[37] BL[36] BL[35] BL[34] BL[33] BL[32] VSS SET_FORM_BUF COL_SELECT0_5[2]
+ SL[47] SL[46] SL[45] SL[44] SL[43] SL[42] SL[41] SL[40] SL[39] SL[38] SL[37] SL[36] SL[35] SL[34] SL[33]
+ SL[32] SET_RST_BUF COL_ADDR0_5_BUF[2] SL_BLOCK_EN_5[2] ARRAY_EN_5_BUF[2] MAN_BUF BL_BLOCK_EN_5[2] WE_BUF
+ WE_5_BUF[2] WE_5_LONG[2] column_block
x2[1] VBL_SET DI_MASK_BUF[1] VDD SLICE_SELECT_5_BUF[1] AVDD VBL_FORM COL_ADDR3_5_BUF[1] BLDIS_BUF[1]
+ ACLK_BUF COL_ADDR2_5_BUF[1] VSL_RESET AVSS COL_ADDR1_5_BUF[1] BL[31] BL[30] BL[29] BL[28] BL[27] BL[26]
+ BL[25] BL[24] BL[23] BL[22] BL[21] BL[20] BL[19] BL[18] BL[17] BL[16] VSS SET_FORM_BUF COL_SELECT0_5[1]
+ SL[31] SL[30] SL[29] SL[28] SL[27] SL[26] SL[25] SL[24] SL[23] SL[22] SL[21] SL[20] SL[19] SL[18] SL[17]
+ SL[16] SET_RST_BUF COL_ADDR0_5_BUF[1] SL_BLOCK_EN_5[1] ARRAY_EN_5_BUF[1] MAN_BUF BL_BLOCK_EN_5[1] WE_BUF
+ WE_5_BUF[1] WE_5_LONG[1] column_block
x2[0] VBL_SET DI_MASK_BUF[0] VDD SLICE_SELECT_5_BUF[0] AVDD VBL_FORM COL_ADDR3_5_BUF[0] BLDIS_BUF[0]
+ ACLK_BUF COL_ADDR2_5_BUF[0] VSL_RESET AVSS COL_ADDR1_5_BUF[0] BL[15] BL[14] BL[13] BL[12] BL[11] BL[10]
+ BL[9] BL[8] BL[7] BL[6] BL[5] BL[4] BL[3] BL[2] BL[1] BL[0] VSS SET_FORM_BUF COL_SELECT0_5[0] SL[15]
+ SL[14] SL[13] SL[12] SL[11] SL[10] SL[9] SL[8] SL[7] SL[6] SL[5] SL[4] SL[3] SL[2] SL[1] SL[0] SET_RST_BUF
+ COL_ADDR0_5_BUF[0] SL_BLOCK_EN_5[0] ARRAY_EN_5_BUF[0] MAN_BUF BL_BLOCK_EN_5[0] WE_BUF WE_5_BUF[0] WE_5_LONG[0]
+ column_block
* noconn WE_5_LONG[15:0]
* noconn SL_BLOCK_EN_5[15:0]
* noconn COL_SELECT0_5[15:0]
* noconn BL_BLOCK_EN_5[15:0]
**.ends
.end
